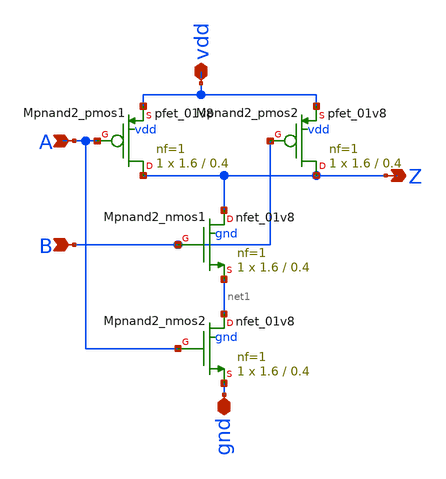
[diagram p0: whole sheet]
** sch_path: sram_4_16_scn4m/pnand2_1.sch
**.subckt pnand2_1 A B Z vdd gnd
*.ipin A
*.ipin B
*.opin Z
*.iopin vdd
*.iopin gnd
XMpnand2_nmos1 Z B net1 gnd sky130_fd_pr__nfet_01v8 L=0.4 W=1.6 nf=1 ad='int((nf+1)/2) * W/nf * 0.29'
+ as='int((nf+2)/2) * W/nf * 0.29' pd='2*int((nf+1)/2) * (W/nf + 0.29)' ps='2*int((nf+2)/2) * (W/nf + 0.29)'
+ nrd='0.29 / W' nrs='0.29 / W' sa=0 sb=0 sd=0 mult=1 m=1
XMpnand2_pmos1 Z A vdd vdd sky130_fd_pr__pfet_01v8 L=0.4 W=1.6 nf=1 ad='int((nf+1)/2) * W/nf * 0.29'
+ as='int((nf+2)/2) * W/nf * 0.29' pd='2*int((nf+1)/2) * (W/nf + 0.29)' ps='2*int((nf+2)/2) * (W/nf + 0.29)'
+ nrd='0.29 / W' nrs='0.29 / W' sa=0 sb=0 sd=0 mult=1 m=1
XMpnand2_pmos2 Z B vdd vdd sky130_fd_pr__pfet_01v8 L=0.4 W=1.6 nf=1 ad='int((nf+1)/2) * W/nf * 0.29'
+ as='int((nf+2)/2) * W/nf * 0.29' pd='2*int((nf+1)/2) * (W/nf + 0.29)' ps='2*int((nf+2)/2) * (W/nf + 0.29)'
+ nrd='0.29 / W' nrs='0.29 / W' sa=0 sb=0 sd=0 mult=1 m=1
XMpnand2_nmos2 net1 A gnd gnd sky130_fd_pr__nfet_01v8 L=0.4 W=1.6 nf=1 ad='int((nf+1)/2) * W/nf * 0.29'
+ as='int((nf+2)/2) * W/nf * 0.29' pd='2*int((nf+1)/2) * (W/nf + 0.29)' ps='2*int((nf+2)/2) * (W/nf + 0.29)'
+ nrd='0.29 / W' nrs='0.29 / W' sa=0 sb=0 sd=0 mult=1 m=1
**.ends
.end
